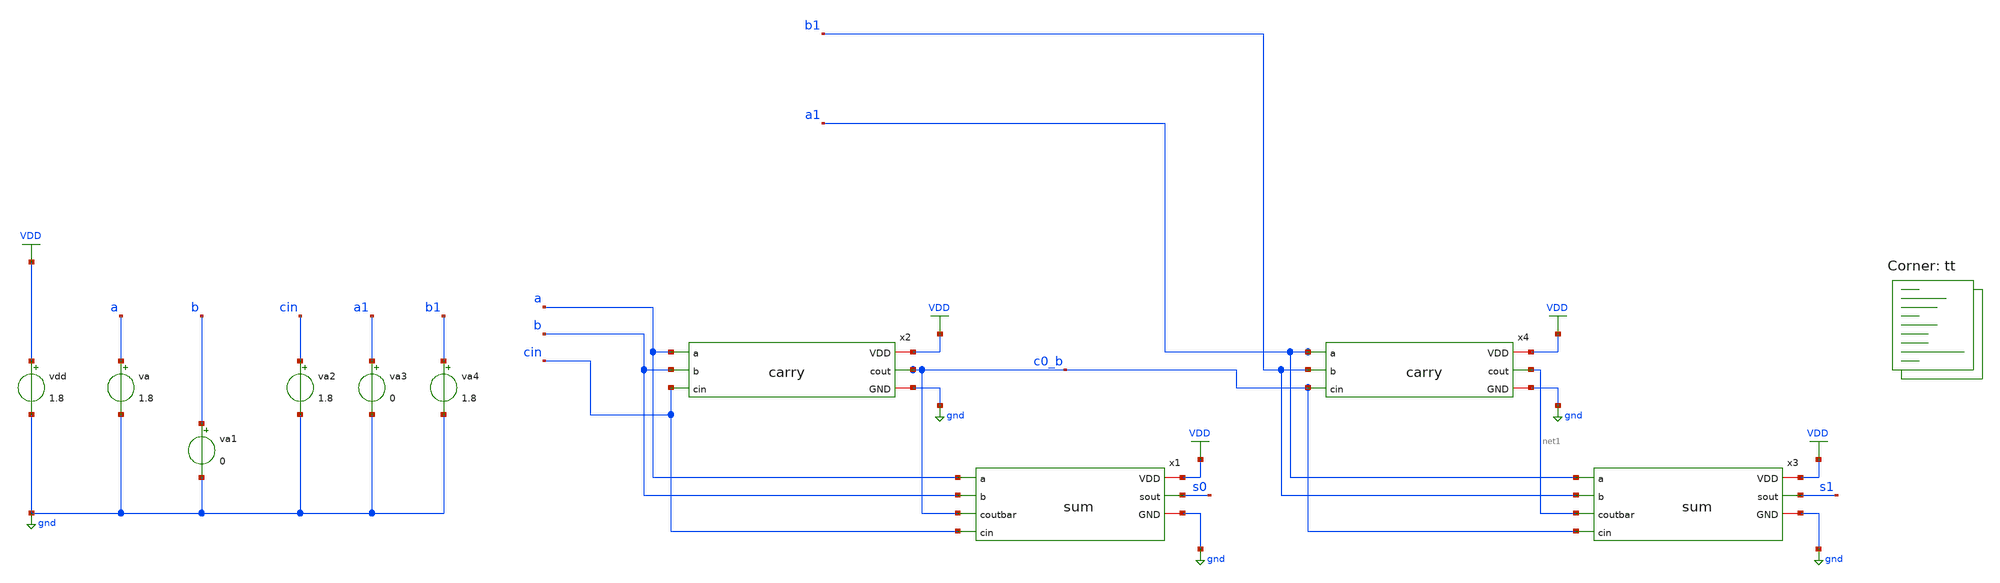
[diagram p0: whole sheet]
** sch_path: assignments/assignment7/assign1a.sch
**.subckt assign1a
x1 VDD a b c0_b cin s0 gnd sum
x2 VDD a b cin c0_b gnd carry
x3 VDD a1 b1 net1 c0_b s1 gnd sum
x4 VDD a1 b1 c0_b net1 gnd carry
vdd VDD gnd 1.8
va a gnd 1.8
va1 b gnd 0
va2 cin gnd 1.8
va3 a1 gnd 0
va4 b1 gnd 1.8
**** begin user architecture code


.include carry_extracted.spice
.control
* alter @va[pulse] = [ 1.8 0 0 0 0 4n 8n]
* alter @va1[pulse] = [ 1.8 0 0 0 0 4n 8n]
alter @va2[pulse] = [ 0 1.8 0 10p 10p 4n 8n ]
* alter @va3[pulse] = [ 1.8 0 0 0 0 4n 8n]
* alter @va4[pulse] = [ 1.8 0 0 0 0 4n 8n]

tran 1p 20n
meas tran delay_cin_net1 TRIG v(cin) VAL=0.9 RISE=3 TARG v(c0_b) VAL=0.9 FALL=3
meas tran delay_cin_s0 TRIG v(cin) VAL=0.9 RISE=3 TARG v(s0) VAL=0.9 RISE=3
plot v(cin) v(s0)
print delay_cin_net1 delay_cin_s0
.endc


.lib $::SKYWATER_MODELS/sky130.lib.spice tt
**** end user architecture code
**.ends

* expanding   symbol:  carry.sym # of pins=6
** sym_path: assignments/assignment7/carry.sym
** sch_path: assignments/assignment7/carry.sch
.subckt carry VDD a b cin cout GND
*.opin cout
*.ipin a
*.iopin VDD
*.iopin GND
*.ipin b
*.ipin cin
XM1 cout cin net3 GND sky130_fd_pr__nfet_01v8 L=0.15 W=0.84 nf=2 ad='int((nf+1)/2) * W/nf * 0.29' as='int((nf+2)/2) * W/nf * 0.29'
+ pd='2*int((nf+1)/2) * (W/nf + 0.29)' ps='2*int((nf+2)/2) * (W/nf + 0.29)' nrd='0.29 / W' nrs='0.29 / W'
+ sa=0 sb=0 sd=0 mult=1 m=1
XM2 net1 b VDD VDD sky130_fd_pr__pfet_01v8 L=0.15 W=1.68 nf=4 ad='int((nf+1)/2) * W/nf * 0.29' as='int((nf+2)/2) * W/nf * 0.29'
+ pd='2*int((nf+1)/2) * (W/nf + 0.29)' ps='2*int((nf+2)/2) * (W/nf + 0.29)' nrd='0.29 / W' nrs='0.29 / W'
+ sa=0 sb=0 sd=0 mult=1 m=1
XM3 net3 a GND GND sky130_fd_pr__nfet_01v8 L=0.15 W=0.84 nf=2 ad='int((nf+1)/2) * W/nf * 0.29' as='int((nf+2)/2) * W/nf * 0.29'
+ pd='2*int((nf+1)/2) * (W/nf + 0.29)' ps='2*int((nf+2)/2) * (W/nf + 0.29)' nrd='0.29 / W' nrs='0.29 / W'
+ sa=0 sb=0 sd=0 mult=1 m=1
XM4 cout cin net1 VDD sky130_fd_pr__pfet_01v8 L=0.15 W=1.68 nf=4 ad='int((nf+1)/2) * W/nf * 0.29' as='int((nf+2)/2) * W/nf * 0.29'
+ pd='2*int((nf+1)/2) * (W/nf + 0.29)' ps='2*int((nf+2)/2) * (W/nf + 0.29)' nrd='0.29 / W' nrs='0.29 / W'
+ sa=0 sb=0 sd=0 mult=1 m=1
XM5 net1 a VDD VDD sky130_fd_pr__pfet_01v8 L=0.15 W=1.68 nf=4 ad='int((nf+1)/2) * W/nf * 0.29' as='int((nf+2)/2) * W/nf * 0.29'
+ pd='2*int((nf+1)/2) * (W/nf + 0.29)' ps='2*int((nf+2)/2) * (W/nf + 0.29)' nrd='0.29 / W' nrs='0.29 / W'
+ sa=0 sb=0 sd=0 mult=1 m=1
XM6 net2 a VDD VDD sky130_fd_pr__pfet_01v8 L=0.15 W=1.68 nf=4 ad='int((nf+1)/2) * W/nf * 0.29' as='int((nf+2)/2) * W/nf * 0.29'
+ pd='2*int((nf+1)/2) * (W/nf + 0.29)' ps='2*int((nf+2)/2) * (W/nf + 0.29)' nrd='0.29 / W' nrs='0.29 / W'
+ sa=0 sb=0 sd=0 mult=1 m=1
XM7 cout b net2 VDD sky130_fd_pr__pfet_01v8 L=0.15 W=1.68 nf=4 ad='int((nf+1)/2) * W/nf * 0.29' as='int((nf+2)/2) * W/nf * 0.29'
+ pd='2*int((nf+1)/2) * (W/nf + 0.29)' ps='2*int((nf+2)/2) * (W/nf + 0.29)' nrd='0.29 / W' nrs='0.29 / W'
+ sa=0 sb=0 sd=0 mult=1 m=1
XM8 net3 b GND GND sky130_fd_pr__nfet_01v8 L=0.15 W=0.84 nf=2 ad='int((nf+1)/2) * W/nf * 0.29' as='int((nf+2)/2) * W/nf * 0.29'
+ pd='2*int((nf+1)/2) * (W/nf + 0.29)' ps='2*int((nf+2)/2) * (W/nf + 0.29)' nrd='0.29 / W' nrs='0.29 / W'
+ sa=0 sb=0 sd=0 mult=1 m=1
XM9 cout a net4 GND sky130_fd_pr__nfet_01v8 L=0.15 W=0.84 nf=2 ad='int((nf+1)/2) * W/nf * 0.29' as='int((nf+2)/2) * W/nf * 0.29'
+ pd='2*int((nf+1)/2) * (W/nf + 0.29)' ps='2*int((nf+2)/2) * (W/nf + 0.29)' nrd='0.29 / W' nrs='0.29 / W'
+ sa=0 sb=0 sd=0 mult=1 m=1
XM10 net4 b GND GND sky130_fd_pr__nfet_01v8 L=0.15 W=0.84 nf=2 ad='int((nf+1)/2) * W/nf * 0.29' as='int((nf+2)/2) * W/nf * 0.29'
+ pd='2*int((nf+1)/2) * (W/nf + 0.29)' ps='2*int((nf+2)/2) * (W/nf + 0.29)' nrd='0.29 / W' nrs='0.29 / W'
+ sa=0 sb=0 sd=0 mult=1 m=1
.ends

.GLOBAL VDD
.GLOBAL gnd
.end
